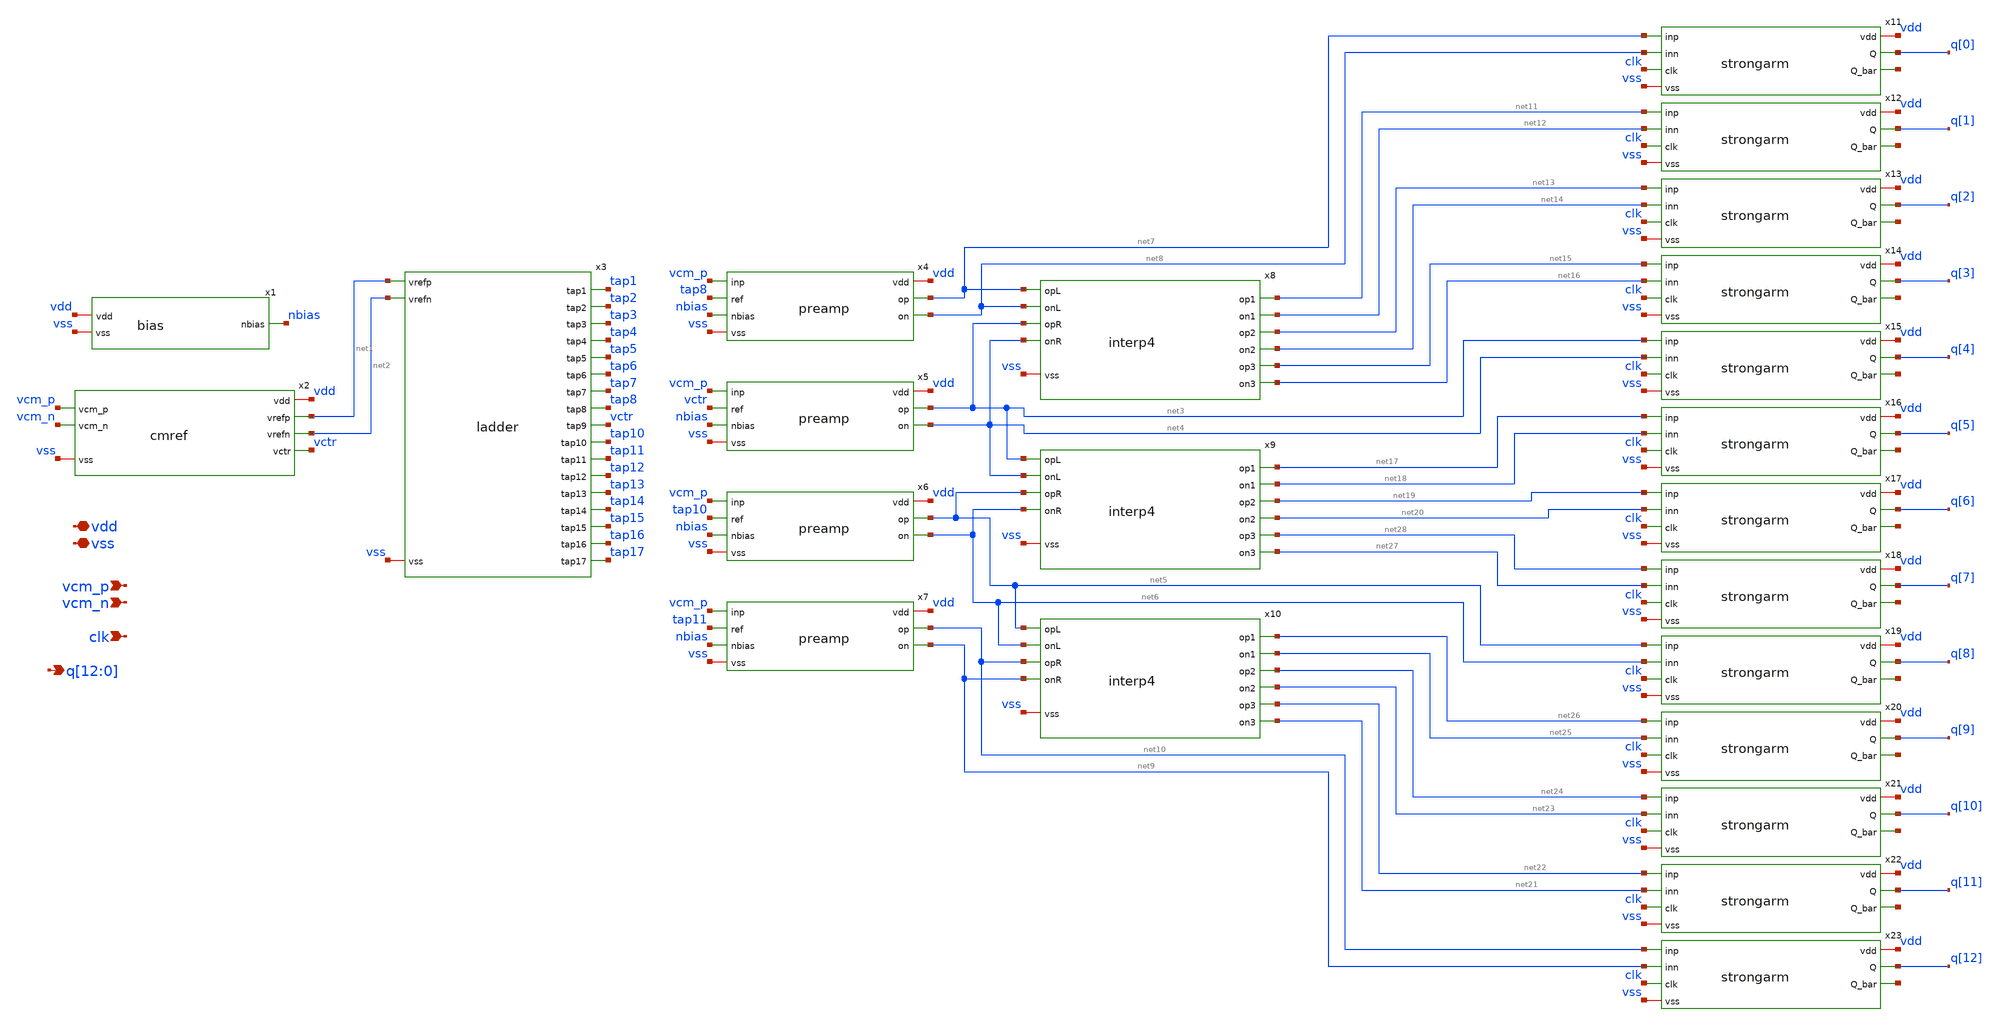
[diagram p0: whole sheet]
** sch_path: blocks/adc/comp-array/block_slice.sch
**.subckt block_slice vdd vss vcm_p vcm_n clk
*+ q[12],q[11],q[10],q[9],q[8],q[7],q[6],q[5],q[4],q[3],q[2],q[1],q[0]
*.iopin vdd
*.iopin vss
*.ipin vcm_p
*.ipin vcm_n
*.ipin clk
*.opin q[12],q[11],q[10],q[9],q[8],q[7],q[6],q[5],q[4],q[3],q[2],q[1],q[0]
x1 vdd vss nbias bias
x2 vdd vss vcm_p vcm_n net1 net2 vctr cmref
x3 net1 net2 tap1 tap2 tap3 tap4 tap5 tap6 tap7 tap8 vctr tap10 tap11 tap12 tap13 tap14 tap15 tap16
+ tap17 vss ladder
x4 vdd vcm_p tap8 nbias net7 net8 vss preamp
x5 vdd vcm_p vctr nbias net3 net4 vss preamp
x6 vdd vcm_p tap10 nbias net5 net6 vss preamp
x7 vdd vcm_p tap11 nbias net10 net9 vss preamp
x8 net7 net8 net3 net4 vss net11 net12 net13 net14 net15 net16 interp4
x9 net3 net4 net5 net6 vss net17 net18 net19 net20 net28 net27 interp4
x10 net5 net6 net10 net9 vss net26 net25 net24 net23 net22 net21 interp4
x11 vdd net7 net8 clk q[0] net29 vss strongarm
x12 vdd net11 net12 clk q[1] net30 vss strongarm
x13 vdd net13 net14 clk q[2] net31 vss strongarm
x14 vdd net15 net16 clk q[3] net32 vss strongarm
x15 vdd net3 net4 clk q[4] net33 vss strongarm
x16 vdd net17 net18 clk q[5] net34 vss strongarm
x17 vdd net19 net20 clk q[6] net35 vss strongarm
x18 vdd net28 net27 clk q[7] net36 vss strongarm
x19 vdd net5 net6 clk q[8] net37 vss strongarm
x20 vdd net26 net25 clk q[9] net38 vss strongarm
x21 vdd net24 net23 clk q[10] net39 vss strongarm
x22 vdd net22 net21 clk q[11] net40 vss strongarm
x23 vdd net10 net9 clk q[12] net41 vss strongarm
**.ends
.end
